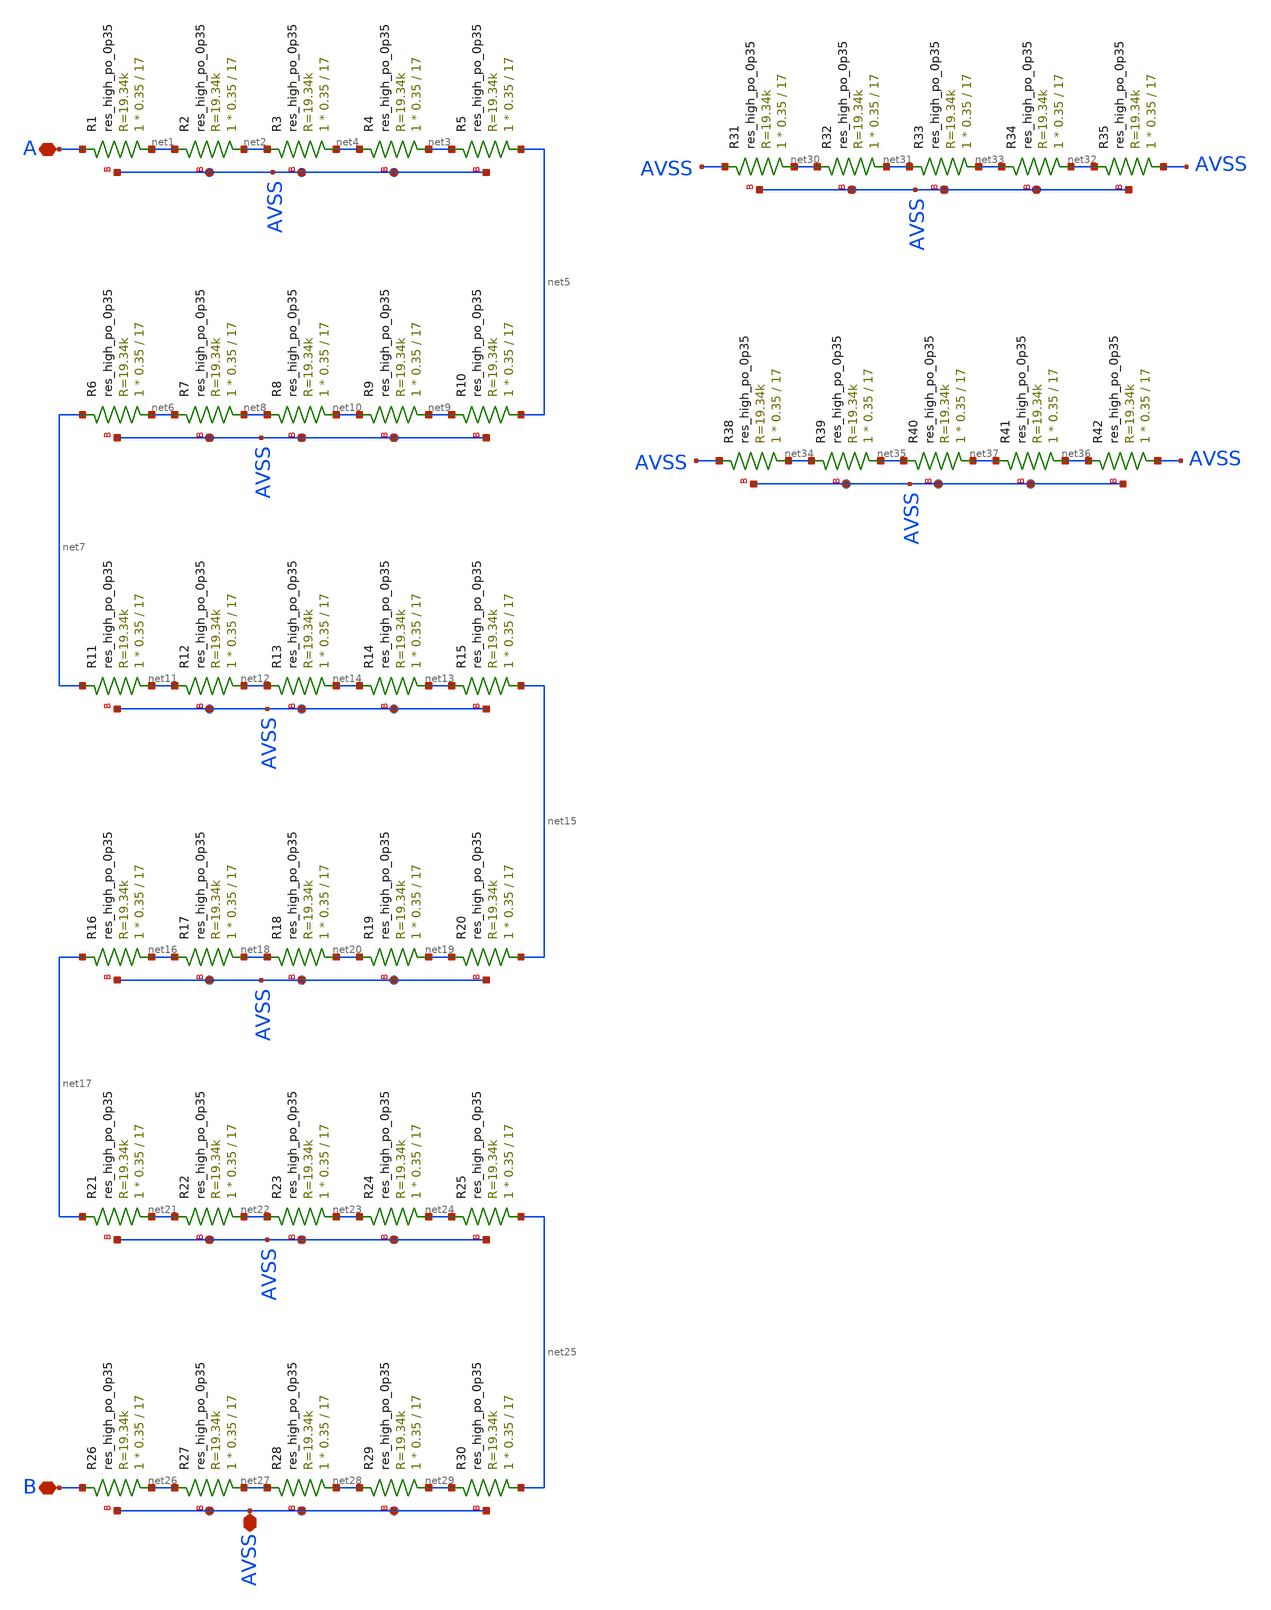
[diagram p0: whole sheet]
** sch_path: magic/resistorstart.sch
**.subckt resistorstart A B AVSS
*.iopin A
*.iopin B
*.iopin AVSS
XR1 net1 A AVSS sky130_fd_pr__res_high_po_0p35 L=17 mult=1 m=1
XR2 net2 net1 AVSS sky130_fd_pr__res_high_po_0p35 L=17 mult=1 m=1
XR3 net4 net2 AVSS sky130_fd_pr__res_high_po_0p35 L=17 mult=1 m=1
XR4 net3 net4 AVSS sky130_fd_pr__res_high_po_0p35 L=17 mult=1 m=1
XR5 net5 net3 AVSS sky130_fd_pr__res_high_po_0p35 L=17 mult=1 m=1
XR6 net6 net7 AVSS sky130_fd_pr__res_high_po_0p35 L=17 mult=1 m=1
XR7 net8 net6 AVSS sky130_fd_pr__res_high_po_0p35 L=17 mult=1 m=1
XR8 net10 net8 AVSS sky130_fd_pr__res_high_po_0p35 L=17 mult=1 m=1
XR9 net9 net10 AVSS sky130_fd_pr__res_high_po_0p35 L=17 mult=1 m=1
XR10 net5 net9 AVSS sky130_fd_pr__res_high_po_0p35 L=17 mult=1 m=1
XR11 net11 net7 AVSS sky130_fd_pr__res_high_po_0p35 L=17 mult=1 m=1
XR12 net12 net11 AVSS sky130_fd_pr__res_high_po_0p35 L=17 mult=1 m=1
XR13 net14 net12 AVSS sky130_fd_pr__res_high_po_0p35 L=17 mult=1 m=1
XR14 net13 net14 AVSS sky130_fd_pr__res_high_po_0p35 L=17 mult=1 m=1
XR15 net15 net13 AVSS sky130_fd_pr__res_high_po_0p35 L=17 mult=1 m=1
XR16 net16 net17 AVSS sky130_fd_pr__res_high_po_0p35 L=17 mult=1 m=1
XR17 net18 net16 AVSS sky130_fd_pr__res_high_po_0p35 L=17 mult=1 m=1
XR18 net20 net18 AVSS sky130_fd_pr__res_high_po_0p35 L=17 mult=1 m=1
XR19 net19 net20 AVSS sky130_fd_pr__res_high_po_0p35 L=17 mult=1 m=1
XR20 net15 net19 AVSS sky130_fd_pr__res_high_po_0p35 L=17 mult=1 m=1
XR21 net21 net17 AVSS sky130_fd_pr__res_high_po_0p35 L=17 mult=1 m=1
XR22 net22 net21 AVSS sky130_fd_pr__res_high_po_0p35 L=17 mult=1 m=1
XR23 net23 net22 AVSS sky130_fd_pr__res_high_po_0p35 L=17 mult=1 m=1
XR24 net24 net23 AVSS sky130_fd_pr__res_high_po_0p35 L=17 mult=1 m=1
XR25 net25 net24 AVSS sky130_fd_pr__res_high_po_0p35 L=17 mult=1 m=1
XR26 net26 B AVSS sky130_fd_pr__res_high_po_0p35 L=17 mult=1 m=1
XR27 net27 net26 AVSS sky130_fd_pr__res_high_po_0p35 L=17 mult=1 m=1
XR28 net28 net27 AVSS sky130_fd_pr__res_high_po_0p35 L=17 mult=1 m=1
XR29 net29 net28 AVSS sky130_fd_pr__res_high_po_0p35 L=17 mult=1 m=1
XR30 net25 net29 AVSS sky130_fd_pr__res_high_po_0p35 L=17 mult=1 m=1
XR31 net30 AVSS AVSS sky130_fd_pr__res_high_po_0p35 L=17 mult=1 m=1
XR32 net31 net30 AVSS sky130_fd_pr__res_high_po_0p35 L=17 mult=1 m=1
XR33 net33 net31 AVSS sky130_fd_pr__res_high_po_0p35 L=17 mult=1 m=1
XR34 net32 net33 AVSS sky130_fd_pr__res_high_po_0p35 L=17 mult=1 m=1
XR35 AVSS net32 AVSS sky130_fd_pr__res_high_po_0p35 L=17 mult=1 m=1
XR38 net34 AVSS AVSS sky130_fd_pr__res_high_po_0p35 L=17 mult=1 m=1
XR39 net35 net34 AVSS sky130_fd_pr__res_high_po_0p35 L=17 mult=1 m=1
XR40 net37 net35 AVSS sky130_fd_pr__res_high_po_0p35 L=17 mult=1 m=1
XR41 net36 net37 AVSS sky130_fd_pr__res_high_po_0p35 L=17 mult=1 m=1
XR42 AVSS net36 AVSS sky130_fd_pr__res_high_po_0p35 L=17 mult=1 m=1
**.ends
.end
